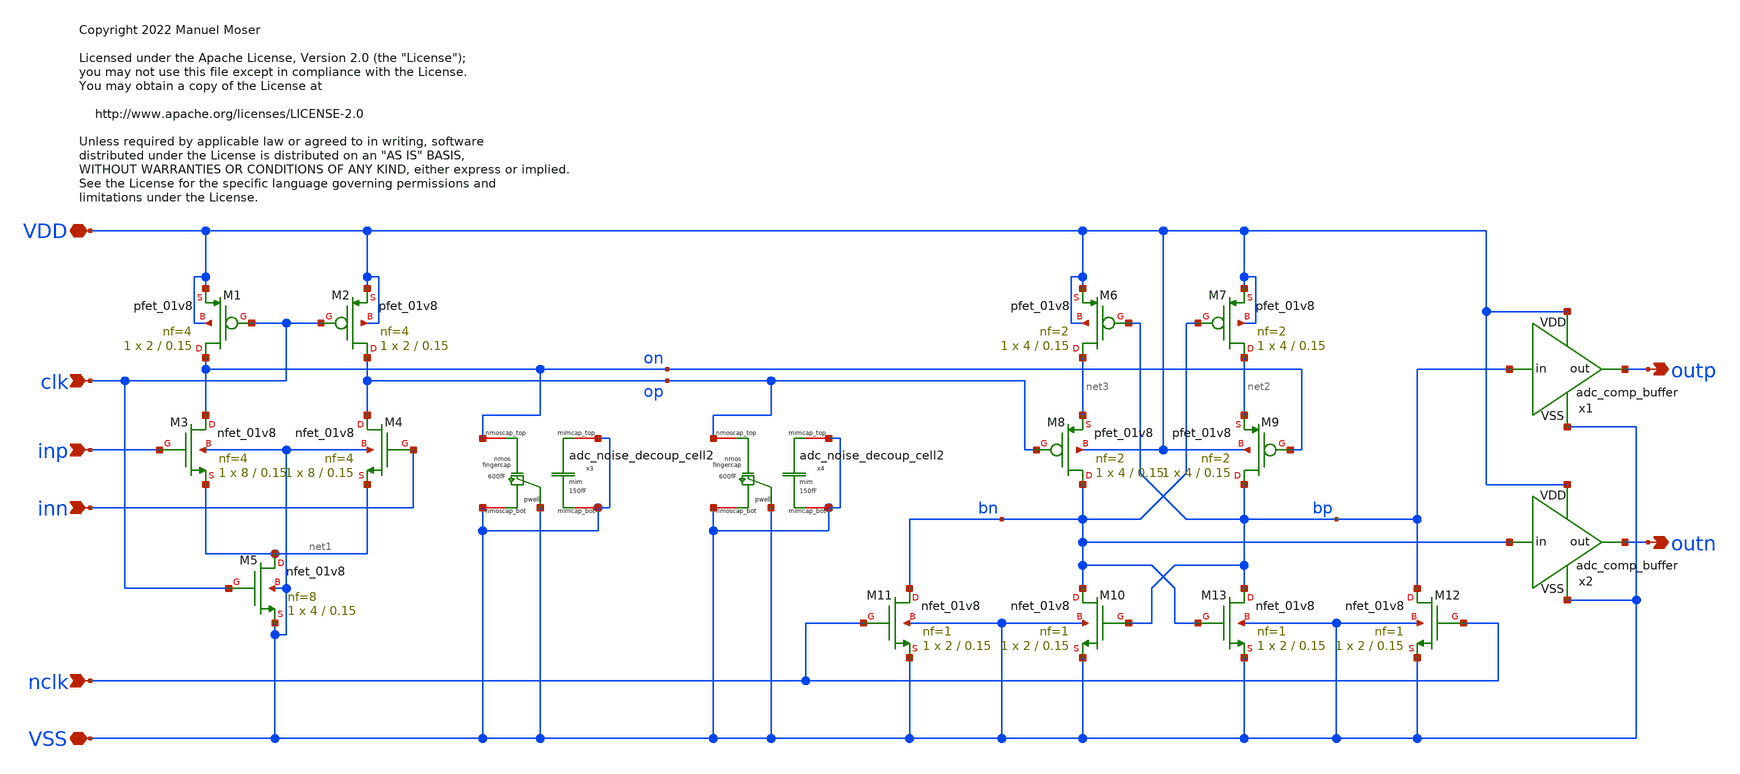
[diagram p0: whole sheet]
** sch_path: xschem/adc_comp_circuit/adc_comp_circuit.sch
* Copyright 2022 Manuel Moser
* Licensed under the Apache License, Version 2.0 (the "License");
**.subckt adc_comp_circuit VDD VSS inp inn clk nclk outp outn
*.iopin VDD
*.iopin VSS
*.ipin inp
*.ipin inn
*.ipin clk
*.ipin nclk
*.opin outp
*.opin outn
XM1 on clk VDD VDD sky130_fd_pr__pfet_01v8 L=0.15 W=2 nf=4 ad='int((nf+1)/2) * W/nf * 0.29' as='int((nf+2)/2) * W/nf * 0.29'
+ pd='2*int((nf+1)/2) * (W/nf + 0.29)' ps='2*int((nf+2)/2) * (W/nf + 0.29)' nrd='0.29 / W' nrs='0.29 / W'
+ sa=0 sb=0 sd=0 mult=1 m=1
XM2 op clk VDD VDD sky130_fd_pr__pfet_01v8 L=0.15 W=2 nf=4 ad='int((nf+1)/2) * W/nf * 0.29' as='int((nf+2)/2) * W/nf * 0.29'
+ pd='2*int((nf+1)/2) * (W/nf + 0.29)' ps='2*int((nf+2)/2) * (W/nf + 0.29)' nrd='0.29 / W' nrs='0.29 / W'
+ sa=0 sb=0 sd=0 mult=1 m=1
XM3 on inp net1 VSS sky130_fd_pr__nfet_01v8 L=0.15 W=8 nf=4 ad='int((nf+1)/2) * W/nf * 0.29' as='int((nf+2)/2) * W/nf * 0.29'
+ pd='2*int((nf+1)/2) * (W/nf + 0.29)' ps='2*int((nf+2)/2) * (W/nf + 0.29)' nrd='0.29 / W' nrs='0.29 / W'
+ sa=0 sb=0 sd=0 mult=1 m=1
XM4 op inn net1 VSS sky130_fd_pr__nfet_01v8 L=0.15 W=8 nf=4 ad='int((nf+1)/2) * W/nf * 0.29' as='int((nf+2)/2) * W/nf * 0.29'
+ pd='2*int((nf+1)/2) * (W/nf + 0.29)' ps='2*int((nf+2)/2) * (W/nf + 0.29)' nrd='0.29 / W' nrs='0.29 / W'
+ sa=0 sb=0 sd=0 mult=1 m=1
XM5 net1 clk VSS VSS sky130_fd_pr__nfet_01v8 L=0.15 W=4 nf=8 ad='int((nf+1)/2) * W/nf * 0.29' as='int((nf+2)/2) * W/nf * 0.29'
+ pd='2*int((nf+1)/2) * (W/nf + 0.29)' ps='2*int((nf+2)/2) * (W/nf + 0.29)' nrd='0.29 / W' nrs='0.29 / W'
+ sa=0 sb=0 sd=0 mult=1 m=1
XM6 net3 bp VDD VDD sky130_fd_pr__pfet_01v8 L=0.15 W=4 nf=2 ad='int((nf+1)/2) * W/nf * 0.29' as='int((nf+2)/2) * W/nf * 0.29'
+ pd='2*int((nf+1)/2) * (W/nf + 0.29)' ps='2*int((nf+2)/2) * (W/nf + 0.29)' nrd='0.29 / W' nrs='0.29 / W'
+ sa=0 sb=0 sd=0 mult=1 m=1
XM7 net2 bn VDD VDD sky130_fd_pr__pfet_01v8 L=0.15 W=4 nf=2 ad='int((nf+1)/2) * W/nf * 0.29' as='int((nf+2)/2) * W/nf * 0.29'
+ pd='2*int((nf+1)/2) * (W/nf + 0.29)' ps='2*int((nf+2)/2) * (W/nf + 0.29)' nrd='0.29 / W' nrs='0.29 / W'
+ sa=0 sb=0 sd=0 mult=1 m=1
XM8 bn op net3 VDD sky130_fd_pr__pfet_01v8 L=0.15 W=4 nf=2 ad='int((nf+1)/2) * W/nf * 0.29' as='int((nf+2)/2) * W/nf * 0.29'
+ pd='2*int((nf+1)/2) * (W/nf + 0.29)' ps='2*int((nf+2)/2) * (W/nf + 0.29)' nrd='0.29 / W' nrs='0.29 / W'
+ sa=0 sb=0 sd=0 mult=1 m=1
XM9 bp on net2 VDD sky130_fd_pr__pfet_01v8 L=0.15 W=4 nf=2 ad='int((nf+1)/2) * W/nf * 0.29' as='int((nf+2)/2) * W/nf * 0.29'
+ pd='2*int((nf+1)/2) * (W/nf + 0.29)' ps='2*int((nf+2)/2) * (W/nf + 0.29)' nrd='0.29 / W' nrs='0.29 / W'
+ sa=0 sb=0 sd=0 mult=1 m=1
XM10 bn bp VSS VSS sky130_fd_pr__nfet_01v8 L=0.15 W=2 nf=1 ad='int((nf+1)/2) * W/nf * 0.29' as='int((nf+2)/2) * W/nf * 0.29'
+ pd='2*int((nf+1)/2) * (W/nf + 0.29)' ps='2*int((nf+2)/2) * (W/nf + 0.29)' nrd='0.29 / W' nrs='0.29 / W'
+ sa=0 sb=0 sd=0 mult=1 m=1
XM11 bn nclk VSS VSS sky130_fd_pr__nfet_01v8 L=0.15 W=2 nf=1 ad='int((nf+1)/2) * W/nf * 0.29' as='int((nf+2)/2) * W/nf * 0.29'
+ pd='2*int((nf+1)/2) * (W/nf + 0.29)' ps='2*int((nf+2)/2) * (W/nf + 0.29)' nrd='0.29 / W' nrs='0.29 / W'
+ sa=0 sb=0 sd=0 mult=1 m=1
XM12 bp nclk VSS VSS sky130_fd_pr__nfet_01v8 L=0.15 W=2 nf=1 ad='int((nf+1)/2) * W/nf * 0.29' as='int((nf+2)/2) * W/nf * 0.29'
+ pd='2*int((nf+1)/2) * (W/nf + 0.29)' ps='2*int((nf+2)/2) * (W/nf + 0.29)' nrd='0.29 / W' nrs='0.29 / W'
+ sa=0 sb=0 sd=0 mult=1 m=1
XM13 bp bn VSS VSS sky130_fd_pr__nfet_01v8 L=0.15 W=2 nf=1 ad='int((nf+1)/2) * W/nf * 0.29' as='int((nf+2)/2) * W/nf * 0.29'
+ pd='2*int((nf+1)/2) * (W/nf + 0.29)' ps='2*int((nf+2)/2) * (W/nf + 0.29)' nrd='0.29 / W' nrs='0.29 / W'
+ sa=0 sb=0 sd=0 mult=1 m=1
x1 VDD VSS bp outp adc_comp_buffer
x2 VDD VSS bn outn adc_comp_buffer
x3 VSS VSS on VSS VSS adc_noise_decoup_cell2
x4 VSS VSS op VSS VSS adc_noise_decoup_cell2
**.ends

* expanding   symbol:  /foss/designs/SKY130_SAR-ADC/xschem/adc_comp_buffer/adc_comp_buffer.sym # of
*+ pins=4
** sym_path: xschem/adc_comp_buffer.sym
** sch_path: xschem/adc_comp_buffer.sch
.subckt adc_comp_buffer VDD VSS in out
*.iopin VDD
*.iopin VSS
*.ipin in
*.opin out
XM5 net1 in VSS VSS sky130_fd_pr__nfet_01v8 L=0.15 W=0.5 nf=1 ad='int((nf+1)/2) * W/nf * 0.29' as='int((nf+2)/2) * W/nf * 0.29'
+ pd='2*int((nf+1)/2) * (W/nf + 0.29)' ps='2*int((nf+2)/2) * (W/nf + 0.29)' nrd='0.29 / W' nrs='0.29 / W'
+ sa=0 sb=0 sd=0 mult=1 m=1
XM1 net1 in VDD VDD sky130_fd_pr__pfet_01v8 L=0.15 W=1 nf=1 ad='int((nf+1)/2) * W/nf * 0.29' as='int((nf+2)/2) * W/nf * 0.29'
+ pd='2*int((nf+1)/2) * (W/nf + 0.29)' ps='2*int((nf+2)/2) * (W/nf + 0.29)' nrd='0.29 / W' nrs='0.29 / W'
+ sa=0 sb=0 sd=0 mult=1 m=1
XM2 out net1 VDD VDD sky130_fd_pr__pfet_01v8 L=0.15 W=2 nf=2 ad='int((nf+1)/2) * W/nf * 0.29' as='int((nf+2)/2) * W/nf * 0.29'
+ pd='2*int((nf+1)/2) * (W/nf + 0.29)' ps='2*int((nf+2)/2) * (W/nf + 0.29)' nrd='0.29 / W' nrs='0.29 / W'
+ sa=0 sb=0 sd=0 mult=1 m=1
XM6 out net1 VSS VSS sky130_fd_pr__nfet_01v8 L=0.15 W=1 nf=2 ad='int((nf+1)/2) * W/nf * 0.29' as='int((nf+2)/2) * W/nf * 0.29'
+ pd='2*int((nf+1)/2) * (W/nf + 0.29)' ps='2*int((nf+2)/2) * (W/nf + 0.29)' nrd='0.29 / W' nrs='0.29 / W'
+ sa=0 sb=0 sd=0 mult=1 m=1
.ends


* expanding   symbol:
*+  /foss/designs/SKY130_SAR-ADC/xschem/adc_noise_decoup_cell/adc_noise_decoup_cell2.sym # of pins=5
** sym_path: xschem/adc_noise_decoup_cell2.sym
** sch_path: xschem/adc_noise_decoup_cell2.sch
.subckt adc_noise_decoup_cell2 mimcap_top mimcap_bot nmoscap_top nmoscap_bot pwell
*.iopin nmoscap_top
*.iopin mimcap_top
*.iopin mimcap_bot
*.iopin nmoscap_bot
*.iopin pwell
XC1 mimcap_top mimcap_bot sky130_fd_pr__cap_mim_m3_1 W=18.9 L=5.1 MF=1 m=1
XC2 nmoscap_top nmoscap_bot pwell sky130_fd_pr__cap_var_lvt W=18.4 L=3.9 VM=1 m=1
.ends

.end
